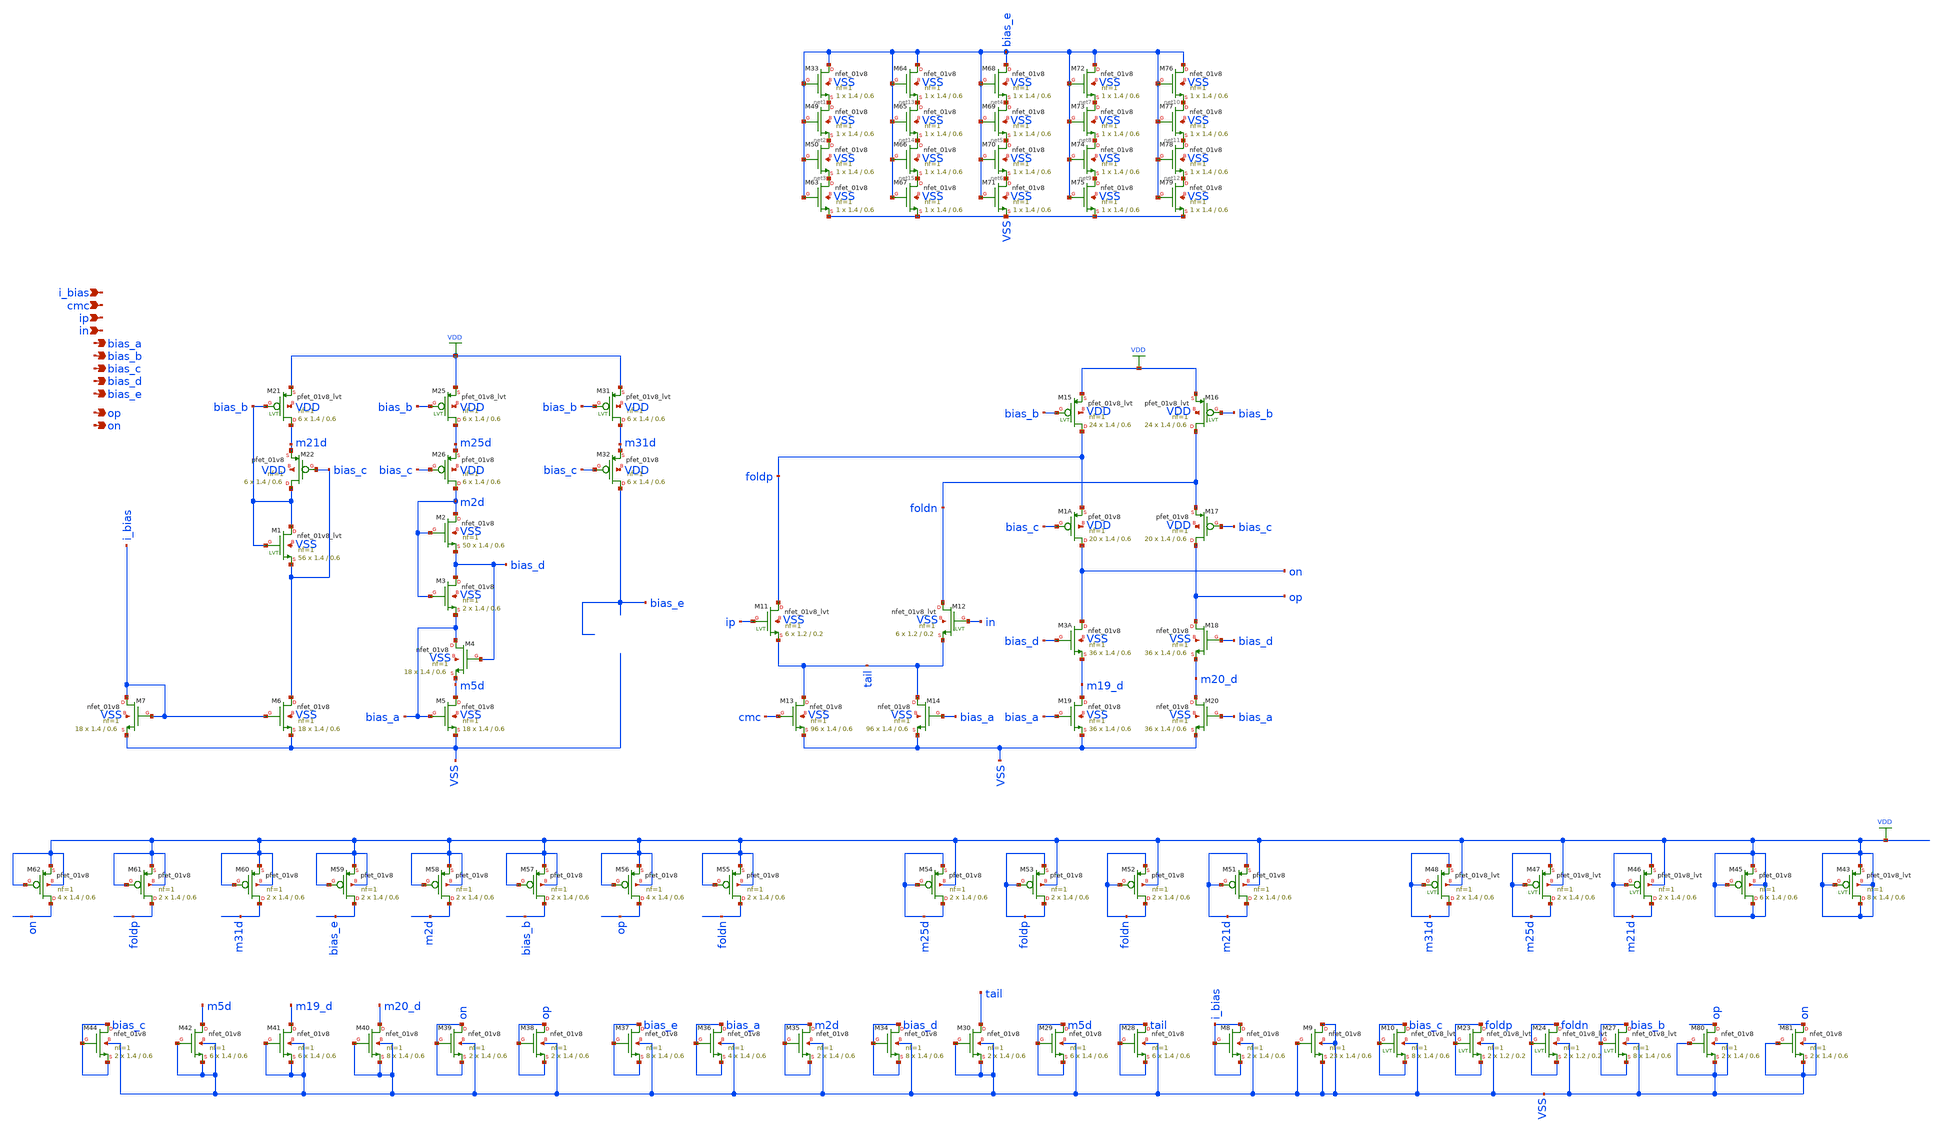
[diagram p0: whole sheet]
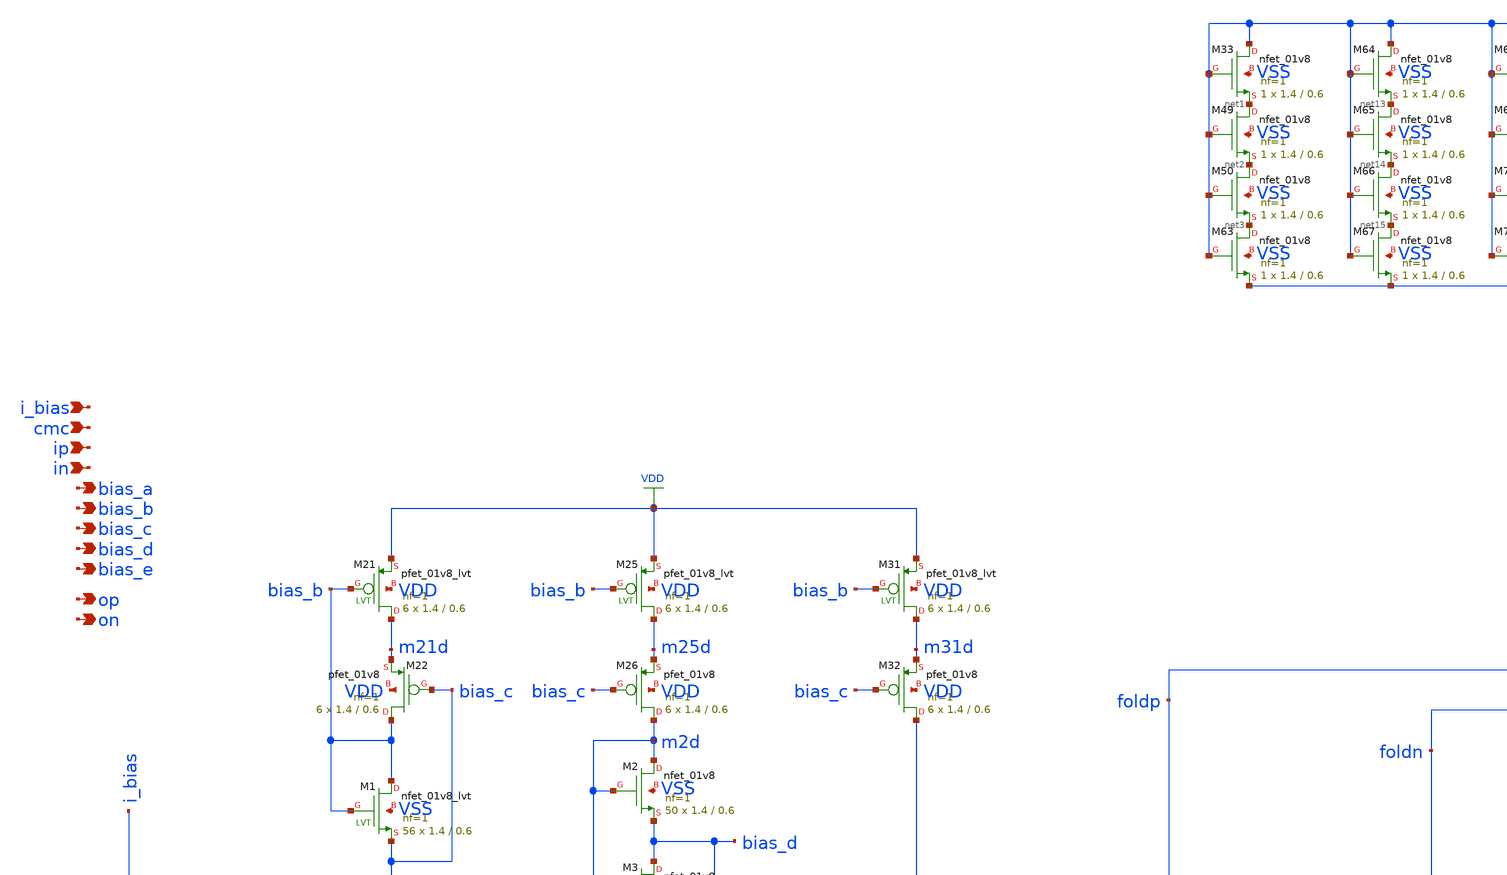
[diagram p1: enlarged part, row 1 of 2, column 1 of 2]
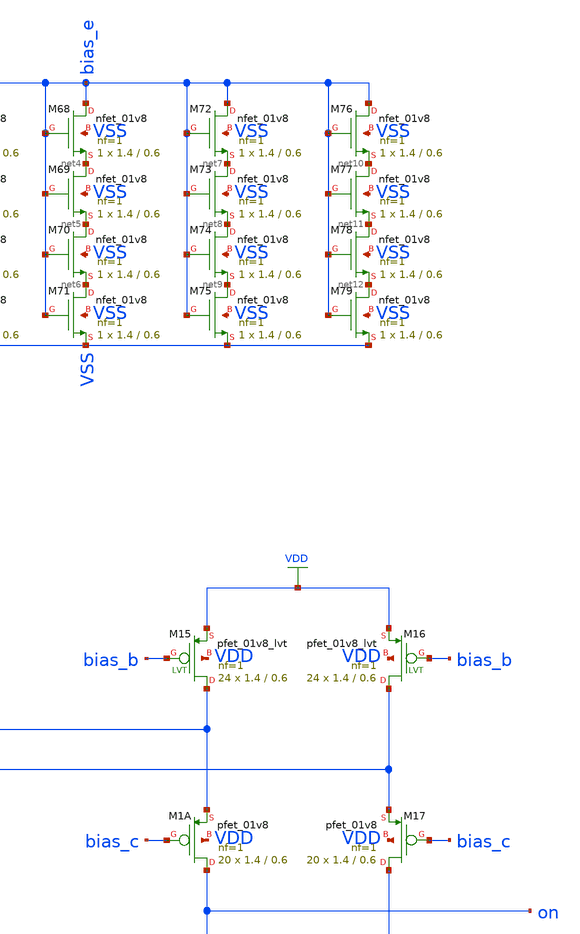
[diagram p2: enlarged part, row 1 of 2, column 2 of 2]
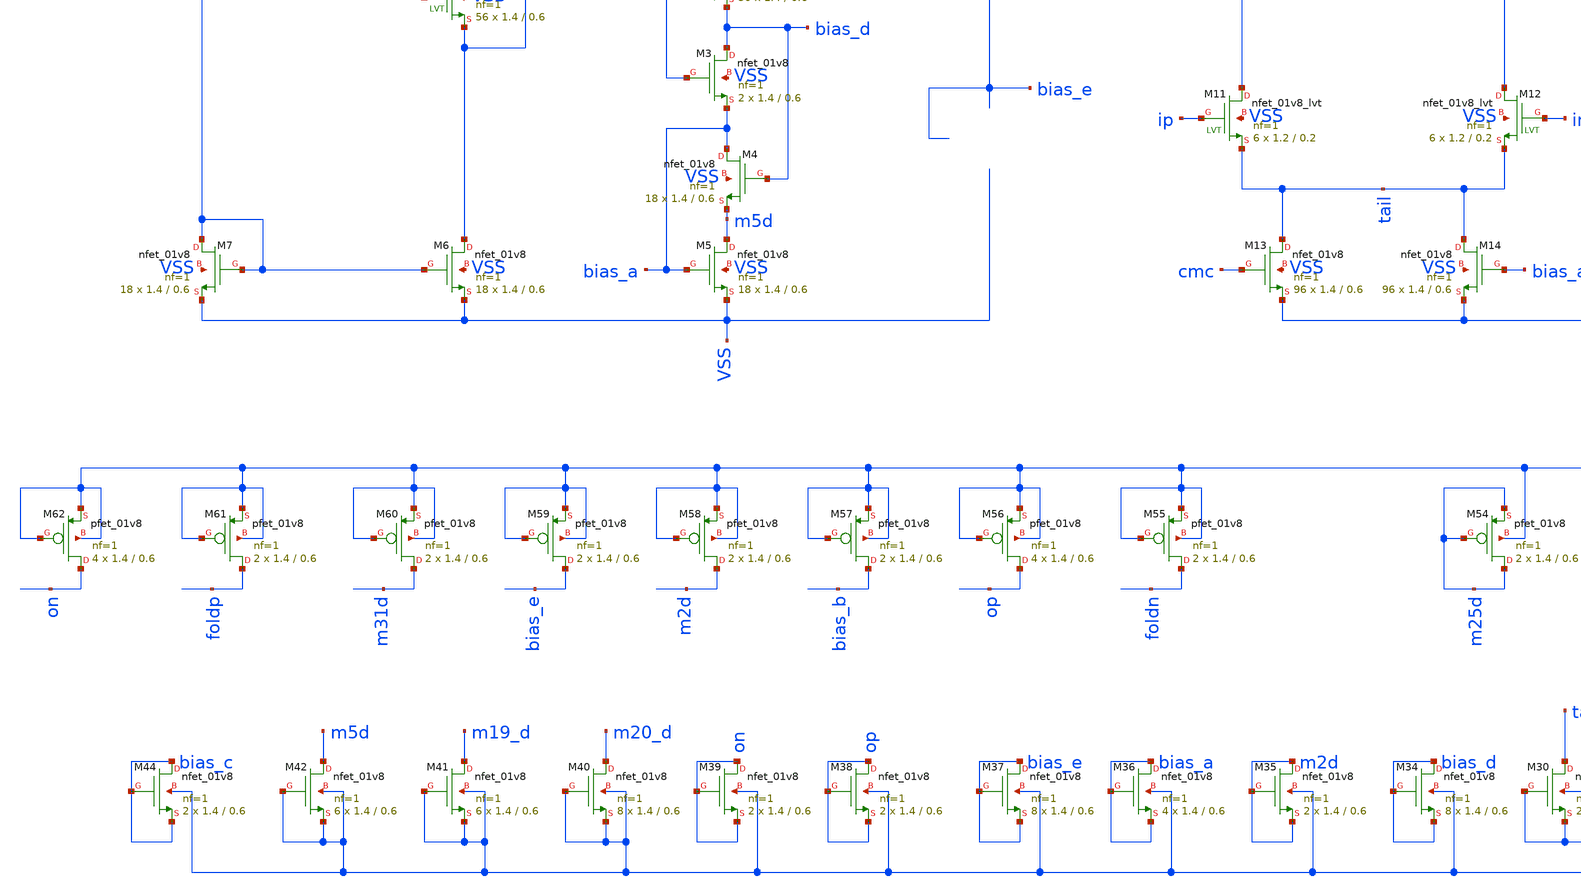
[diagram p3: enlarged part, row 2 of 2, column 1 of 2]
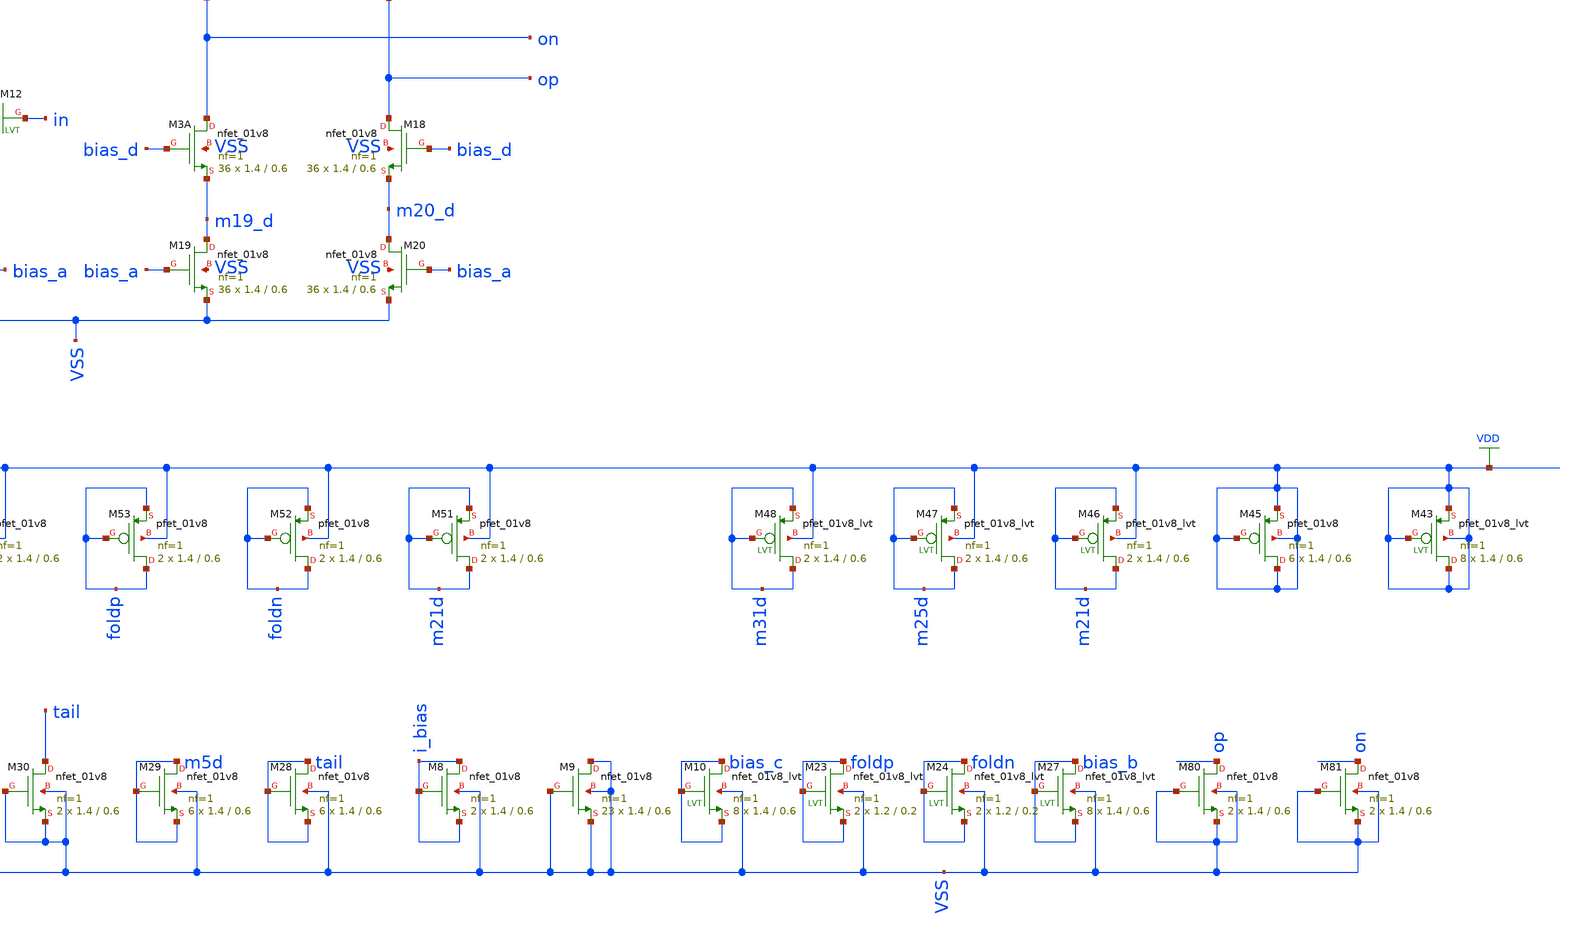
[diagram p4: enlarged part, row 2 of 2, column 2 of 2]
** sch_path: design/analog_modulator/schematic/ota_lvs.sch
**.subckt ota_lvs ip in op on i_bias bias_e bias_a bias_b bias_c bias_d cmc
*.ipin ip
*.ipin in
*.opin op
*.opin on
*.ipin i_bias
*.opin bias_e
*.opin bias_a
*.opin bias_b
*.opin bias_c
*.opin bias_d
*.ipin cmc
XM22 bias_b bias_c m21d VDD sky130_fd_pr__pfet_01v8 L=0.6 W=1.4 nf=1 ad='int((nf+1)/2) * W/nf * 0.29'
+ as='int((nf+2)/2) * W/nf * 0.29' pd='2*int((nf+1)/2) * (W/nf + 0.29)' ps='2*int((nf+2)/2) * (W/nf + 0.29)'
+ nrd='0.29 / W' nrs='0.29 / W' sa=0 sb=0 sd=0 mult=6 m=6
XM26 m2d bias_c m25d VDD sky130_fd_pr__pfet_01v8 L=0.6 W=1.4 nf=1 ad='int((nf+1)/2) * W/nf * 0.29' as='int((nf+2)/2) * W/nf * 0.29'
+ pd='2*int((nf+1)/2) * (W/nf + 0.29)' ps='2*int((nf+2)/2) * (W/nf + 0.29)' nrd='0.29 / W' nrs='0.29 / W'
+ sa=0 sb=0 sd=0 mult=6 m=6
XM32 bias_e bias_c m31d VDD sky130_fd_pr__pfet_01v8 L=0.6 W=1.4 nf=1 ad='int((nf+1)/2) * W/nf * 0.29'
+ as='int((nf+2)/2) * W/nf * 0.29' pd='2*int((nf+1)/2) * (W/nf + 0.29)' ps='2*int((nf+2)/2) * (W/nf + 0.29)'
+ nrd='0.29 / W' nrs='0.29 / W' sa=0 sb=0 sd=0 mult=6 m=6
XM33 bias_e bias_e net1 VSS sky130_fd_pr__nfet_01v8 L=0.6 W=1.4 nf=1 ad='int((nf+1)/2) * W/nf * 0.29'
+ as='int((nf+2)/2) * W/nf * 0.29' pd='2*int((nf+1)/2) * (W/nf + 0.29)' ps='2*int((nf+2)/2) * (W/nf + 0.29)'
+ nrd='0.29 / W' nrs='0.29 / W' sa=0 sb=0 sd=0 mult=1 m=1
XM21 m21d bias_b VDD VDD sky130_fd_pr__pfet_01v8_lvt L=0.6 W=1.4 nf=1 ad='int((nf+1)/2) * W/nf * 0.29'
+ as='int((nf+2)/2) * W/nf * 0.29' pd='2*int((nf+1)/2) * (W/nf + 0.29)' ps='2*int((nf+2)/2) * (W/nf + 0.29)'
+ nrd='0.29 / W' nrs='0.29 / W' sa=0 sb=0 sd=0 mult=6 m=6
XM25 m25d bias_b VDD VDD sky130_fd_pr__pfet_01v8_lvt L=0.6 W=1.4 nf=1 ad='int((nf+1)/2) * W/nf * 0.29'
+ as='int((nf+2)/2) * W/nf * 0.29' pd='2*int((nf+1)/2) * (W/nf + 0.29)' ps='2*int((nf+2)/2) * (W/nf + 0.29)'
+ nrd='0.29 / W' nrs='0.29 / W' sa=0 sb=0 sd=0 mult=6 m=6
XM31 m31d bias_b VDD VDD sky130_fd_pr__pfet_01v8_lvt L=0.6 W=1.4 nf=1 ad='int((nf+1)/2) * W/nf * 0.29'
+ as='int((nf+2)/2) * W/nf * 0.29' pd='2*int((nf+1)/2) * (W/nf + 0.29)' ps='2*int((nf+2)/2) * (W/nf + 0.29)'
+ nrd='0.29 / W' nrs='0.29 / W' sa=0 sb=0 sd=0 mult=6 m=6
XM1 bias_b bias_b bias_c VSS sky130_fd_pr__nfet_01v8_lvt L=0.6 W=1.4 nf=1 ad='int((nf+1)/2) * W/nf * 0.29'
+ as='int((nf+2)/2) * W/nf * 0.29' pd='2*int((nf+1)/2) * (W/nf + 0.29)' ps='2*int((nf+2)/2) * (W/nf + 0.29)'
+ nrd='0.29 / W' nrs='0.29 / W' sa=0 sb=0 sd=0 mult=56 m=56
XM2 m2d m2d bias_d VSS sky130_fd_pr__nfet_01v8 L=0.6 W=1.4 nf=1 ad='int((nf+1)/2) * W/nf * 0.29' as='int((nf+2)/2) * W/nf * 0.29'
+ pd='2*int((nf+1)/2) * (W/nf + 0.29)' ps='2*int((nf+2)/2) * (W/nf + 0.29)' nrd='0.29 / W' nrs='0.29 / W'
+ sa=0 sb=0 sd=0 mult=50 m=50
XM3 bias_d m2d bias_a VSS sky130_fd_pr__nfet_01v8 L=0.6 W=1.4 nf=1 ad='int((nf+1)/2) * W/nf * 0.29' as='int((nf+2)/2) * W/nf * 0.29'
+ pd='2*int((nf+1)/2) * (W/nf + 0.29)' ps='2*int((nf+2)/2) * (W/nf + 0.29)' nrd='0.29 / W' nrs='0.29 / W'
+ sa=0 sb=0 sd=0 mult=2 m=2
XM4 bias_a bias_d m5d VSS sky130_fd_pr__nfet_01v8 L=0.6 W=1.4 nf=1 ad='int((nf+1)/2) * W/nf * 0.29' as='int((nf+2)/2) * W/nf * 0.29'
+ pd='2*int((nf+1)/2) * (W/nf + 0.29)' ps='2*int((nf+2)/2) * (W/nf + 0.29)' nrd='0.29 / W' nrs='0.29 / W'
+ sa=0 sb=0 sd=0 mult=18 m=18
XM5 m5d bias_a VSS VSS sky130_fd_pr__nfet_01v8 L=0.6 W=1.4 nf=1 ad='int((nf+1)/2) * W/nf * 0.29' as='int((nf+2)/2) * W/nf * 0.29'
+ pd='2*int((nf+1)/2) * (W/nf + 0.29)' ps='2*int((nf+2)/2) * (W/nf + 0.29)' nrd='0.29 / W' nrs='0.29 / W'
+ sa=0 sb=0 sd=0 mult=18 m=18
XM6 bias_c i_bias VSS VSS sky130_fd_pr__nfet_01v8 L=0.6 W=1.4 nf=1 ad='int((nf+1)/2) * W/nf * 0.29' as='int((nf+2)/2) * W/nf * 0.29'
+ pd='2*int((nf+1)/2) * (W/nf + 0.29)' ps='2*int((nf+2)/2) * (W/nf + 0.29)' nrd='0.29 / W' nrs='0.29 / W'
+ sa=0 sb=0 sd=0 mult=18 m=18
XM7 i_bias i_bias VSS VSS sky130_fd_pr__nfet_01v8 L=0.6 W=1.4 nf=1 ad='int((nf+1)/2) * W/nf * 0.29' as='int((nf+2)/2) * W/nf * 0.29'
+ pd='2*int((nf+1)/2) * (W/nf + 0.29)' ps='2*int((nf+2)/2) * (W/nf + 0.29)' nrd='0.29 / W' nrs='0.29 / W'
+ sa=0 sb=0 sd=0 mult=18 m=18
XM8 i_bias i_bias i_bias VSS sky130_fd_pr__nfet_01v8 L=0.6 W=1.4 nf=1 ad='int((nf+1)/2) * W/nf * 0.29'
+ as='int((nf+2)/2) * W/nf * 0.29' pd='2*int((nf+1)/2) * (W/nf + 0.29)' ps='2*int((nf+2)/2) * (W/nf + 0.29)'
+ nrd='0.29 / W' nrs='0.29 / W' sa=0 sb=0 sd=0 mult=2 m=2
XM9 VSS VSS VSS VSS sky130_fd_pr__nfet_01v8 L=0.6 W=1.4 nf=1 ad='int((nf+1)/2) * W/nf * 0.29' as='int((nf+2)/2) * W/nf * 0.29'
+ pd='2*int((nf+1)/2) * (W/nf + 0.29)' ps='2*int((nf+2)/2) * (W/nf + 0.29)' nrd='0.29 / W' nrs='0.29 / W'
+ sa=0 sb=0 sd=0 mult=23 m=23
XM10 bias_c bias_c bias_c VSS sky130_fd_pr__nfet_01v8_lvt L=0.6 W=1.4 nf=1 ad='int((nf+1)/2) * W/nf * 0.29'
+ as='int((nf+2)/2) * W/nf * 0.29' pd='2*int((nf+1)/2) * (W/nf + 0.29)' ps='2*int((nf+2)/2) * (W/nf + 0.29)'
+ nrd='0.29 / W' nrs='0.29 / W' sa=0 sb=0 sd=0 mult=8 m=8
XM11 foldp ip tail VSS sky130_fd_pr__nfet_01v8_lvt L=0.2 W=1.2 nf=1 ad='int((nf+1)/2) * W/nf * 0.29'
+ as='int((nf+2)/2) * W/nf * 0.29' pd='2*int((nf+1)/2) * (W/nf + 0.29)' ps='2*int((nf+2)/2) * (W/nf + 0.29)'
+ nrd='0.29 / W' nrs='0.29 / W' sa=0 sb=0 sd=0 mult=6 m=6
XM12 foldn in tail VSS sky130_fd_pr__nfet_01v8_lvt L=0.2 W=1.2 nf=1 ad='int((nf+1)/2) * W/nf * 0.29'
+ as='int((nf+2)/2) * W/nf * 0.29' pd='2*int((nf+1)/2) * (W/nf + 0.29)' ps='2*int((nf+2)/2) * (W/nf + 0.29)'
+ nrd='0.29 / W' nrs='0.29 / W' sa=0 sb=0 sd=0 mult=6 m=6
XM13 tail cmc VSS VSS sky130_fd_pr__nfet_01v8 L=0.6 W=1.4 nf=1 ad='int((nf+1)/2) * W/nf * 0.29' as='int((nf+2)/2) * W/nf * 0.29'
+ pd='2*int((nf+1)/2) * (W/nf + 0.29)' ps='2*int((nf+2)/2) * (W/nf + 0.29)' nrd='0.29 / W' nrs='0.29 / W'
+ sa=0 sb=0 sd=0 mult=96 m=96
XM14 tail bias_a VSS VSS sky130_fd_pr__nfet_01v8 L=0.6 W=1.4 nf=1 ad='int((nf+1)/2) * W/nf * 0.29' as='int((nf+2)/2) * W/nf * 0.29'
+ pd='2*int((nf+1)/2) * (W/nf + 0.29)' ps='2*int((nf+2)/2) * (W/nf + 0.29)' nrd='0.29 / W' nrs='0.29 / W'
+ sa=0 sb=0 sd=0 mult=96 m=96
XM15 foldp bias_b VDD VDD sky130_fd_pr__pfet_01v8_lvt L=0.6 W=1.4 nf=1 ad='int((nf+1)/2) * W/nf * 0.29'
+ as='int((nf+2)/2) * W/nf * 0.29' pd='2*int((nf+1)/2) * (W/nf + 0.29)' ps='2*int((nf+2)/2) * (W/nf + 0.29)'
+ nrd='0.29 / W' nrs='0.29 / W' sa=0 sb=0 sd=0 mult=24 m=24
XM16 foldn bias_b VDD VDD sky130_fd_pr__pfet_01v8_lvt L=0.6 W=1.4 nf=1 ad='int((nf+1)/2) * W/nf * 0.29'
+ as='int((nf+2)/2) * W/nf * 0.29' pd='2*int((nf+1)/2) * (W/nf + 0.29)' ps='2*int((nf+2)/2) * (W/nf + 0.29)'
+ nrd='0.29 / W' nrs='0.29 / W' sa=0 sb=0 sd=0 mult=24 m=24
XM1A on bias_c foldp VDD sky130_fd_pr__pfet_01v8 L=0.6 W=1.4 nf=1 ad='int((nf+1)/2) * W/nf * 0.29' as='int((nf+2)/2) * W/nf * 0.29'
+ pd='2*int((nf+1)/2) * (W/nf + 0.29)' ps='2*int((nf+2)/2) * (W/nf + 0.29)' nrd='0.29 / W' nrs='0.29 / W'
+ sa=0 sb=0 sd=0 mult=20 m=20
XM17 op bias_c foldn VDD sky130_fd_pr__pfet_01v8 L=0.6 W=1.4 nf=1 ad='int((nf+1)/2) * W/nf * 0.29' as='int((nf+2)/2) * W/nf * 0.29'
+ pd='2*int((nf+1)/2) * (W/nf + 0.29)' ps='2*int((nf+2)/2) * (W/nf + 0.29)' nrd='0.29 / W' nrs='0.29 / W'
+ sa=0 sb=0 sd=0 mult=20 m=20
XM3A on bias_d m19_d VSS sky130_fd_pr__nfet_01v8 L=0.6 W=1.4 nf=1 ad='int((nf+1)/2) * W/nf * 0.29' as='int((nf+2)/2) * W/nf * 0.29'
+ pd='2*int((nf+1)/2) * (W/nf + 0.29)' ps='2*int((nf+2)/2) * (W/nf + 0.29)' nrd='0.29 / W' nrs='0.29 / W'
+ sa=0 sb=0 sd=0 mult=36 m=36
XM18 op bias_d m20_d VSS sky130_fd_pr__nfet_01v8 L=0.6 W=1.4 nf=1 ad='int((nf+1)/2) * W/nf * 0.29' as='int((nf+2)/2) * W/nf * 0.29'
+ pd='2*int((nf+1)/2) * (W/nf + 0.29)' ps='2*int((nf+2)/2) * (W/nf + 0.29)' nrd='0.29 / W' nrs='0.29 / W'
+ sa=0 sb=0 sd=0 mult=36 m=36
XM19 m19_d bias_a VSS VSS sky130_fd_pr__nfet_01v8 L=0.6 W=1.4 nf=1 ad='int((nf+1)/2) * W/nf * 0.29' as='int((nf+2)/2) * W/nf * 0.29'
+ pd='2*int((nf+1)/2) * (W/nf + 0.29)' ps='2*int((nf+2)/2) * (W/nf + 0.29)' nrd='0.29 / W' nrs='0.29 / W'
+ sa=0 sb=0 sd=0 mult=36 m=36
XM20 m20_d bias_a VSS VSS sky130_fd_pr__nfet_01v8 L=0.6 W=1.4 nf=1 ad='int((nf+1)/2) * W/nf * 0.29' as='int((nf+2)/2) * W/nf * 0.29'
+ pd='2*int((nf+1)/2) * (W/nf + 0.29)' ps='2*int((nf+2)/2) * (W/nf + 0.29)' nrd='0.29 / W' nrs='0.29 / W'
+ sa=0 sb=0 sd=0 mult=36 m=36
XM23 foldp foldp foldp VSS sky130_fd_pr__nfet_01v8_lvt L=0.2 W=1.2 nf=1 ad='int((nf+1)/2) * W/nf * 0.29'
+ as='int((nf+2)/2) * W/nf * 0.29' pd='2*int((nf+1)/2) * (W/nf + 0.29)' ps='2*int((nf+2)/2) * (W/nf + 0.29)'
+ nrd='0.29 / W' nrs='0.29 / W' sa=0 sb=0 sd=0 mult=2 m=2
XM24 foldn foldn foldn VSS sky130_fd_pr__nfet_01v8_lvt L=0.2 W=1.2 nf=1 ad='int((nf+1)/2) * W/nf * 0.29'
+ as='int((nf+2)/2) * W/nf * 0.29' pd='2*int((nf+1)/2) * (W/nf + 0.29)' ps='2*int((nf+2)/2) * (W/nf + 0.29)'
+ nrd='0.29 / W' nrs='0.29 / W' sa=0 sb=0 sd=0 mult=2 m=2
XM27 bias_b bias_b bias_b VSS sky130_fd_pr__nfet_01v8_lvt L=0.6 W=1.4 nf=1 ad='int((nf+1)/2) * W/nf * 0.29'
+ as='int((nf+2)/2) * W/nf * 0.29' pd='2*int((nf+1)/2) * (W/nf + 0.29)' ps='2*int((nf+2)/2) * (W/nf + 0.29)'
+ nrd='0.29 / W' nrs='0.29 / W' sa=0 sb=0 sd=0 mult=8 m=8
XM28 tail tail tail VSS sky130_fd_pr__nfet_01v8 L=0.6 W=1.4 nf=1 ad='int((nf+1)/2) * W/nf * 0.29' as='int((nf+2)/2) * W/nf * 0.29'
+ pd='2*int((nf+1)/2) * (W/nf + 0.29)' ps='2*int((nf+2)/2) * (W/nf + 0.29)' nrd='0.29 / W' nrs='0.29 / W'
+ sa=0 sb=0 sd=0 mult=6 m=6
XM29 m5d m5d m5d VSS sky130_fd_pr__nfet_01v8 L=0.6 W=1.4 nf=1 ad='int((nf+1)/2) * W/nf * 0.29' as='int((nf+2)/2) * W/nf * 0.29'
+ pd='2*int((nf+1)/2) * (W/nf + 0.29)' ps='2*int((nf+2)/2) * (W/nf + 0.29)' nrd='0.29 / W' nrs='0.29 / W'
+ sa=0 sb=0 sd=0 mult=6 m=6
XM30 tail VSS VSS VSS sky130_fd_pr__nfet_01v8 L=0.6 W=1.4 nf=1 ad='int((nf+1)/2) * W/nf * 0.29' as='int((nf+2)/2) * W/nf * 0.29'
+ pd='2*int((nf+1)/2) * (W/nf + 0.29)' ps='2*int((nf+2)/2) * (W/nf + 0.29)' nrd='0.29 / W' nrs='0.29 / W'
+ sa=0 sb=0 sd=0 mult=2 m=2
XM34 bias_d bias_d bias_d VSS sky130_fd_pr__nfet_01v8 L=0.6 W=1.4 nf=1 ad='int((nf+1)/2) * W/nf * 0.29'
+ as='int((nf+2)/2) * W/nf * 0.29' pd='2*int((nf+1)/2) * (W/nf + 0.29)' ps='2*int((nf+2)/2) * (W/nf + 0.29)'
+ nrd='0.29 / W' nrs='0.29 / W' sa=0 sb=0 sd=0 mult=8 m=8
XM35 m2d m2d m2d VSS sky130_fd_pr__nfet_01v8 L=0.6 W=1.4 nf=1 ad='int((nf+1)/2) * W/nf * 0.29' as='int((nf+2)/2) * W/nf * 0.29'
+ pd='2*int((nf+1)/2) * (W/nf + 0.29)' ps='2*int((nf+2)/2) * (W/nf + 0.29)' nrd='0.29 / W' nrs='0.29 / W'
+ sa=0 sb=0 sd=0 mult=2 m=2
XM36 bias_a bias_a bias_a VSS sky130_fd_pr__nfet_01v8 L=0.6 W=1.4 nf=1 ad='int((nf+1)/2) * W/nf * 0.29'
+ as='int((nf+2)/2) * W/nf * 0.29' pd='2*int((nf+1)/2) * (W/nf + 0.29)' ps='2*int((nf+2)/2) * (W/nf + 0.29)'
+ nrd='0.29 / W' nrs='0.29 / W' sa=0 sb=0 sd=0 mult=4 m=4
XM37 bias_e bias_e bias_e VSS sky130_fd_pr__nfet_01v8 L=0.6 W=1.4 nf=1 ad='int((nf+1)/2) * W/nf * 0.29'
+ as='int((nf+2)/2) * W/nf * 0.29' pd='2*int((nf+1)/2) * (W/nf + 0.29)' ps='2*int((nf+2)/2) * (W/nf + 0.29)'
+ nrd='0.29 / W' nrs='0.29 / W' sa=0 sb=0 sd=0 mult=8 m=8
XM38 op op op VSS sky130_fd_pr__nfet_01v8 L=0.6 W=1.4 nf=1 ad='int((nf+1)/2) * W/nf * 0.29' as='int((nf+2)/2) * W/nf * 0.29'
+ pd='2*int((nf+1)/2) * (W/nf + 0.29)' ps='2*int((nf+2)/2) * (W/nf + 0.29)' nrd='0.29 / W' nrs='0.29 / W'
+ sa=0 sb=0 sd=0 mult=2 m=2
XM39 on on on VSS sky130_fd_pr__nfet_01v8 L=0.6 W=1.4 nf=1 ad='int((nf+1)/2) * W/nf * 0.29' as='int((nf+2)/2) * W/nf * 0.29'
+ pd='2*int((nf+1)/2) * (W/nf + 0.29)' ps='2*int((nf+2)/2) * (W/nf + 0.29)' nrd='0.29 / W' nrs='0.29 / W'
+ sa=0 sb=0 sd=0 mult=2 m=2
XM40 m20_d VSS VSS VSS sky130_fd_pr__nfet_01v8 L=0.6 W=1.4 nf=1 ad='int((nf+1)/2) * W/nf * 0.29' as='int((nf+2)/2) * W/nf * 0.29'
+ pd='2*int((nf+1)/2) * (W/nf + 0.29)' ps='2*int((nf+2)/2) * (W/nf + 0.29)' nrd='0.29 / W' nrs='0.29 / W'
+ sa=0 sb=0 sd=0 mult=8 m=8
XM41 m19_d VSS VSS VSS sky130_fd_pr__nfet_01v8 L=0.6 W=1.4 nf=1 ad='int((nf+1)/2) * W/nf * 0.29' as='int((nf+2)/2) * W/nf * 0.29'
+ pd='2*int((nf+1)/2) * (W/nf + 0.29)' ps='2*int((nf+2)/2) * (W/nf + 0.29)' nrd='0.29 / W' nrs='0.29 / W'
+ sa=0 sb=0 sd=0 mult=6 m=6
XM42 m5d VSS VSS VSS sky130_fd_pr__nfet_01v8 L=0.6 W=1.4 nf=1 ad='int((nf+1)/2) * W/nf * 0.29' as='int((nf+2)/2) * W/nf * 0.29'
+ pd='2*int((nf+1)/2) * (W/nf + 0.29)' ps='2*int((nf+2)/2) * (W/nf + 0.29)' nrd='0.29 / W' nrs='0.29 / W'
+ sa=0 sb=0 sd=0 mult=6 m=6
XM43 VDD VDD VDD VDD sky130_fd_pr__pfet_01v8_lvt L=0.6 W=1.4 nf=1 ad='int((nf+1)/2) * W/nf * 0.29' as='int((nf+2)/2) * W/nf * 0.29'
+ pd='2*int((nf+1)/2) * (W/nf + 0.29)' ps='2*int((nf+2)/2) * (W/nf + 0.29)' nrd='0.29 / W' nrs='0.29 / W'
+ sa=0 sb=0 sd=0 mult=8 m=8
XM44 bias_c bias_c bias_c VSS sky130_fd_pr__nfet_01v8 L=0.6 W=1.4 nf=1 ad='int((nf+1)/2) * W/nf * 0.29'
+ as='int((nf+2)/2) * W/nf * 0.29' pd='2*int((nf+1)/2) * (W/nf + 0.29)' ps='2*int((nf+2)/2) * (W/nf + 0.29)'
+ nrd='0.29 / W' nrs='0.29 / W' sa=0 sb=0 sd=0 mult=2 m=2
XM45 VDD VDD VDD VDD sky130_fd_pr__pfet_01v8 L=0.6 W=1.4 nf=1 ad='int((nf+1)/2) * W/nf * 0.29' as='int((nf+2)/2) * W/nf * 0.29'
+ pd='2*int((nf+1)/2) * (W/nf + 0.29)' ps='2*int((nf+2)/2) * (W/nf + 0.29)' nrd='0.29 / W' nrs='0.29 / W'
+ sa=0 sb=0 sd=0 mult=6 m=6
XM46 m21d m21d m21d VDD sky130_fd_pr__pfet_01v8_lvt L=0.6 W=1.4 nf=1 ad='int((nf+1)/2) * W/nf * 0.29'
+ as='int((nf+2)/2) * W/nf * 0.29' pd='2*int((nf+1)/2) * (W/nf + 0.29)' ps='2*int((nf+2)/2) * (W/nf + 0.29)'
+ nrd='0.29 / W' nrs='0.29 / W' sa=0 sb=0 sd=0 mult=2 m=2
XM47 m25d m25d m25d VDD sky130_fd_pr__pfet_01v8_lvt L=0.6 W=1.4 nf=1 ad='int((nf+1)/2) * W/nf * 0.29'
+ as='int((nf+2)/2) * W/nf * 0.29' pd='2*int((nf+1)/2) * (W/nf + 0.29)' ps='2*int((nf+2)/2) * (W/nf + 0.29)'
+ nrd='0.29 / W' nrs='0.29 / W' sa=0 sb=0 sd=0 mult=2 m=2
XM48 m31d m31d m31d VDD sky130_fd_pr__pfet_01v8_lvt L=0.6 W=1.4 nf=1 ad='int((nf+1)/2) * W/nf * 0.29'
+ as='int((nf+2)/2) * W/nf * 0.29' pd='2*int((nf+1)/2) * (W/nf + 0.29)' ps='2*int((nf+2)/2) * (W/nf + 0.29)'
+ nrd='0.29 / W' nrs='0.29 / W' sa=0 sb=0 sd=0 mult=2 m=2
XM51 m21d m21d m21d VDD sky130_fd_pr__pfet_01v8 L=0.6 W=1.4 nf=1 ad='int((nf+1)/2) * W/nf * 0.29' as='int((nf+2)/2) * W/nf * 0.29'
+ pd='2*int((nf+1)/2) * (W/nf + 0.29)' ps='2*int((nf+2)/2) * (W/nf + 0.29)' nrd='0.29 / W' nrs='0.29 / W'
+ sa=0 sb=0 sd=0 mult=2 m=2
XM52 foldn foldn foldn VDD sky130_fd_pr__pfet_01v8 L=0.6 W=1.4 nf=1 ad='int((nf+1)/2) * W/nf * 0.29'
+ as='int((nf+2)/2) * W/nf * 0.29' pd='2*int((nf+1)/2) * (W/nf + 0.29)' ps='2*int((nf+2)/2) * (W/nf + 0.29)'
+ nrd='0.29 / W' nrs='0.29 / W' sa=0 sb=0 sd=0 mult=2 m=2
XM53 foldp foldp foldp VDD sky130_fd_pr__pfet_01v8 L=0.6 W=1.4 nf=1 ad='int((nf+1)/2) * W/nf * 0.29'
+ as='int((nf+2)/2) * W/nf * 0.29' pd='2*int((nf+1)/2) * (W/nf + 0.29)' ps='2*int((nf+2)/2) * (W/nf + 0.29)'
+ nrd='0.29 / W' nrs='0.29 / W' sa=0 sb=0 sd=0 mult=2 m=2
XM54 m25d m25d m25d VDD sky130_fd_pr__pfet_01v8 L=0.6 W=1.4 nf=1 ad='int((nf+1)/2) * W/nf * 0.29' as='int((nf+2)/2) * W/nf * 0.29'
+ pd='2*int((nf+1)/2) * (W/nf + 0.29)' ps='2*int((nf+2)/2) * (W/nf + 0.29)' nrd='0.29 / W' nrs='0.29 / W'
+ sa=0 sb=0 sd=0 mult=2 m=2
XM55 foldn VDD VDD VDD sky130_fd_pr__pfet_01v8 L=0.6 W=1.4 nf=1 ad='int((nf+1)/2) * W/nf * 0.29' as='int((nf+2)/2) * W/nf * 0.29'
+ pd='2*int((nf+1)/2) * (W/nf + 0.29)' ps='2*int((nf+2)/2) * (W/nf + 0.29)' nrd='0.29 / W' nrs='0.29 / W'
+ sa=0 sb=0 sd=0 mult=2 m=2
XM56 op VDD VDD VDD sky130_fd_pr__pfet_01v8 L=0.6 W=1.4 nf=1 ad='int((nf+1)/2) * W/nf * 0.29' as='int((nf+2)/2) * W/nf * 0.29'
+ pd='2*int((nf+1)/2) * (W/nf + 0.29)' ps='2*int((nf+2)/2) * (W/nf + 0.29)' nrd='0.29 / W' nrs='0.29 / W'
+ sa=0 sb=0 sd=0 mult=4 m=4
XM57 bias_b VDD VDD VDD sky130_fd_pr__pfet_01v8 L=0.6 W=1.4 nf=1 ad='int((nf+1)/2) * W/nf * 0.29' as='int((nf+2)/2) * W/nf * 0.29'
+ pd='2*int((nf+1)/2) * (W/nf + 0.29)' ps='2*int((nf+2)/2) * (W/nf + 0.29)' nrd='0.29 / W' nrs='0.29 / W'
+ sa=0 sb=0 sd=0 mult=2 m=2
XM58 m2d VDD VDD VDD sky130_fd_pr__pfet_01v8 L=0.6 W=1.4 nf=1 ad='int((nf+1)/2) * W/nf * 0.29' as='int((nf+2)/2) * W/nf * 0.29'
+ pd='2*int((nf+1)/2) * (W/nf + 0.29)' ps='2*int((nf+2)/2) * (W/nf + 0.29)' nrd='0.29 / W' nrs='0.29 / W'
+ sa=0 sb=0 sd=0 mult=2 m=2
XM59 bias_e VDD VDD VDD sky130_fd_pr__pfet_01v8 L=0.6 W=1.4 nf=1 ad='int((nf+1)/2) * W/nf * 0.29' as='int((nf+2)/2) * W/nf * 0.29'
+ pd='2*int((nf+1)/2) * (W/nf + 0.29)' ps='2*int((nf+2)/2) * (W/nf + 0.29)' nrd='0.29 / W' nrs='0.29 / W'
+ sa=0 sb=0 sd=0 mult=2 m=2
XM60 m31d VDD VDD VDD sky130_fd_pr__pfet_01v8 L=0.6 W=1.4 nf=1 ad='int((nf+1)/2) * W/nf * 0.29' as='int((nf+2)/2) * W/nf * 0.29'
+ pd='2*int((nf+1)/2) * (W/nf + 0.29)' ps='2*int((nf+2)/2) * (W/nf + 0.29)' nrd='0.29 / W' nrs='0.29 / W'
+ sa=0 sb=0 sd=0 mult=2 m=2
XM61 foldp VDD VDD VDD sky130_fd_pr__pfet_01v8 L=0.6 W=1.4 nf=1 ad='int((nf+1)/2) * W/nf * 0.29' as='int((nf+2)/2) * W/nf * 0.29'
+ pd='2*int((nf+1)/2) * (W/nf + 0.29)' ps='2*int((nf+2)/2) * (W/nf + 0.29)' nrd='0.29 / W' nrs='0.29 / W'
+ sa=0 sb=0 sd=0 mult=2 m=2
XM62 on VDD VDD VDD sky130_fd_pr__pfet_01v8 L=0.6 W=1.4 nf=1 ad='int((nf+1)/2) * W/nf * 0.29' as='int((nf+2)/2) * W/nf * 0.29'
+ pd='2*int((nf+1)/2) * (W/nf + 0.29)' ps='2*int((nf+2)/2) * (W/nf + 0.29)' nrd='0.29 / W' nrs='0.29 / W'
+ sa=0 sb=0 sd=0 mult=4 m=4
XM49 net1 bias_e net2 VSS sky130_fd_pr__nfet_01v8 L=0.6 W=1.4 nf=1 ad='int((nf+1)/2) * W/nf * 0.29' as='int((nf+2)/2) * W/nf * 0.29'
+ pd='2*int((nf+1)/2) * (W/nf + 0.29)' ps='2*int((nf+2)/2) * (W/nf + 0.29)' nrd='0.29 / W' nrs='0.29 / W'
+ sa=0 sb=0 sd=0 mult=1 m=1
XM50 net2 bias_e net3 VSS sky130_fd_pr__nfet_01v8 L=0.6 W=1.4 nf=1 ad='int((nf+1)/2) * W/nf * 0.29' as='int((nf+2)/2) * W/nf * 0.29'
+ pd='2*int((nf+1)/2) * (W/nf + 0.29)' ps='2*int((nf+2)/2) * (W/nf + 0.29)' nrd='0.29 / W' nrs='0.29 / W'
+ sa=0 sb=0 sd=0 mult=1 m=1
XM63 net3 bias_e VSS VSS sky130_fd_pr__nfet_01v8 L=0.6 W=1.4 nf=1 ad='int((nf+1)/2) * W/nf * 0.29' as='int((nf+2)/2) * W/nf * 0.29'
+ pd='2*int((nf+1)/2) * (W/nf + 0.29)' ps='2*int((nf+2)/2) * (W/nf + 0.29)' nrd='0.29 / W' nrs='0.29 / W'
+ sa=0 sb=0 sd=0 mult=1 m=1
XM68 bias_e bias_e net4 VSS sky130_fd_pr__nfet_01v8 L=0.6 W=1.4 nf=1 ad='int((nf+1)/2) * W/nf * 0.29'
+ as='int((nf+2)/2) * W/nf * 0.29' pd='2*int((nf+1)/2) * (W/nf + 0.29)' ps='2*int((nf+2)/2) * (W/nf + 0.29)'
+ nrd='0.29 / W' nrs='0.29 / W' sa=0 sb=0 sd=0 mult=1 m=1
XM69 net4 bias_e net5 VSS sky130_fd_pr__nfet_01v8 L=0.6 W=1.4 nf=1 ad='int((nf+1)/2) * W/nf * 0.29' as='int((nf+2)/2) * W/nf * 0.29'
+ pd='2*int((nf+1)/2) * (W/nf + 0.29)' ps='2*int((nf+2)/2) * (W/nf + 0.29)' nrd='0.29 / W' nrs='0.29 / W'
+ sa=0 sb=0 sd=0 mult=1 m=1
XM70 net5 bias_e net6 VSS sky130_fd_pr__nfet_01v8 L=0.6 W=1.4 nf=1 ad='int((nf+1)/2) * W/nf * 0.29' as='int((nf+2)/2) * W/nf * 0.29'
+ pd='2*int((nf+1)/2) * (W/nf + 0.29)' ps='2*int((nf+2)/2) * (W/nf + 0.29)' nrd='0.29 / W' nrs='0.29 / W'
+ sa=0 sb=0 sd=0 mult=1 m=1
XM71 net6 bias_e VSS VSS sky130_fd_pr__nfet_01v8 L=0.6 W=1.4 nf=1 ad='int((nf+1)/2) * W/nf * 0.29' as='int((nf+2)/2) * W/nf * 0.29'
+ pd='2*int((nf+1)/2) * (W/nf + 0.29)' ps='2*int((nf+2)/2) * (W/nf + 0.29)' nrd='0.29 / W' nrs='0.29 / W'
+ sa=0 sb=0 sd=0 mult=1 m=1
XM72 bias_e bias_e net7 VSS sky130_fd_pr__nfet_01v8 L=0.6 W=1.4 nf=1 ad='int((nf+1)/2) * W/nf * 0.29'
+ as='int((nf+2)/2) * W/nf * 0.29' pd='2*int((nf+1)/2) * (W/nf + 0.29)' ps='2*int((nf+2)/2) * (W/nf + 0.29)'
+ nrd='0.29 / W' nrs='0.29 / W' sa=0 sb=0 sd=0 mult=1 m=1
XM73 net7 bias_e net8 VSS sky130_fd_pr__nfet_01v8 L=0.6 W=1.4 nf=1 ad='int((nf+1)/2) * W/nf * 0.29' as='int((nf+2)/2) * W/nf * 0.29'
+ pd='2*int((nf+1)/2) * (W/nf + 0.29)' ps='2*int((nf+2)/2) * (W/nf + 0.29)' nrd='0.29 / W' nrs='0.29 / W'
+ sa=0 sb=0 sd=0 mult=1 m=1
XM74 net8 bias_e net9 VSS sky130_fd_pr__nfet_01v8 L=0.6 W=1.4 nf=1 ad='int((nf+1)/2) * W/nf * 0.29' as='int((nf+2)/2) * W/nf * 0.29'
+ pd='2*int((nf+1)/2) * (W/nf + 0.29)' ps='2*int((nf+2)/2) * (W/nf + 0.29)' nrd='0.29 / W' nrs='0.29 / W'
+ sa=0 sb=0 sd=0 mult=1 m=1
XM75 net9 bias_e VSS VSS sky130_fd_pr__nfet_01v8 L=0.6 W=1.4 nf=1 ad='int((nf+1)/2) * W/nf * 0.29' as='int((nf+2)/2) * W/nf * 0.29'
+ pd='2*int((nf+1)/2) * (W/nf + 0.29)' ps='2*int((nf+2)/2) * (W/nf + 0.29)' nrd='0.29 / W' nrs='0.29 / W'
+ sa=0 sb=0 sd=0 mult=1 m=1
XM76 bias_e bias_e net10 VSS sky130_fd_pr__nfet_01v8 L=0.6 W=1.4 nf=1 ad='int((nf+1)/2) * W/nf * 0.29'
+ as='int((nf+2)/2) * W/nf * 0.29' pd='2*int((nf+1)/2) * (W/nf + 0.29)' ps='2*int((nf+2)/2) * (W/nf + 0.29)'
+ nrd='0.29 / W' nrs='0.29 / W' sa=0 sb=0 sd=0 mult=1 m=1
XM77 net10 bias_e net11 VSS sky130_fd_pr__nfet_01v8 L=0.6 W=1.4 nf=1 ad='int((nf+1)/2) * W/nf * 0.29'
+ as='int((nf+2)/2) * W/nf * 0.29' pd='2*int((nf+1)/2) * (W/nf + 0.29)' ps='2*int((nf+2)/2) * (W/nf + 0.29)'
+ nrd='0.29 / W' nrs='0.29 / W' sa=0 sb=0 sd=0 mult=1 m=1
XM78 net11 bias_e net12 VSS sky130_fd_pr__nfet_01v8 L=0.6 W=1.4 nf=1 ad='int((nf+1)/2) * W/nf * 0.29'
+ as='int((nf+2)/2) * W/nf * 0.29' pd='2*int((nf+1)/2) * (W/nf + 0.29)' ps='2*int((nf+2)/2) * (W/nf + 0.29)'
+ nrd='0.29 / W' nrs='0.29 / W' sa=0 sb=0 sd=0 mult=1 m=1
XM79 net12 bias_e VSS VSS sky130_fd_pr__nfet_01v8 L=0.6 W=1.4 nf=1 ad='int((nf+1)/2) * W/nf * 0.29' as='int((nf+2)/2) * W/nf * 0.29'
+ pd='2*int((nf+1)/2) * (W/nf + 0.29)' ps='2*int((nf+2)/2) * (W/nf + 0.29)' nrd='0.29 / W' nrs='0.29 / W'
+ sa=0 sb=0 sd=0 mult=1 m=1
XM64 bias_e bias_e net13 VSS sky130_fd_pr__nfet_01v8 L=0.6 W=1.4 nf=1 ad='int((nf+1)/2) * W/nf * 0.29'
+ as='int((nf+2)/2) * W/nf * 0.29' pd='2*int((nf+1)/2) * (W/nf + 0.29)' ps='2*int((nf+2)/2) * (W/nf + 0.29)'
+ nrd='0.29 / W' nrs='0.29 / W' sa=0 sb=0 sd=0 mult=1 m=1
XM65 net13 bias_e net14 VSS sky130_fd_pr__nfet_01v8 L=0.6 W=1.4 nf=1 ad='int((nf+1)/2) * W/nf * 0.29'
+ as='int((nf+2)/2) * W/nf * 0.29' pd='2*int((nf+1)/2) * (W/nf + 0.29)' ps='2*int((nf+2)/2) * (W/nf + 0.29)'
+ nrd='0.29 / W' nrs='0.29 / W' sa=0 sb=0 sd=0 mult=1 m=1
XM66 net14 bias_e net15 VSS sky130_fd_pr__nfet_01v8 L=0.6 W=1.4 nf=1 ad='int((nf+1)/2) * W/nf * 0.29'
+ as='int((nf+2)/2) * W/nf * 0.29' pd='2*int((nf+1)/2) * (W/nf + 0.29)' ps='2*int((nf+2)/2) * (W/nf + 0.29)'
+ nrd='0.29 / W' nrs='0.29 / W' sa=0 sb=0 sd=0 mult=1 m=1
XM67 net15 bias_e VSS VSS sky130_fd_pr__nfet_01v8 L=0.6 W=1.4 nf=1 ad='int((nf+1)/2) * W/nf * 0.29' as='int((nf+2)/2) * W/nf * 0.29'
+ pd='2*int((nf+1)/2) * (W/nf + 0.29)' ps='2*int((nf+2)/2) * (W/nf + 0.29)' nrd='0.29 / W' nrs='0.29 / W'
+ sa=0 sb=0 sd=0 mult=1 m=1
XM80 op VSS VSS VSS sky130_fd_pr__nfet_01v8 L=0.6 W=1.4 nf=1 ad='int((nf+1)/2) * W/nf * 0.29' as='int((nf+2)/2) * W/nf * 0.29'
+ pd='2*int((nf+1)/2) * (W/nf + 0.29)' ps='2*int((nf+2)/2) * (W/nf + 0.29)' nrd='0.29 / W' nrs='0.29 / W'
+ sa=0 sb=0 sd=0 mult=2 m=2
XM81 on VSS VSS VSS sky130_fd_pr__nfet_01v8 L=0.6 W=1.4 nf=1 ad='int((nf+1)/2) * W/nf * 0.29' as='int((nf+2)/2) * W/nf * 0.29'
+ pd='2*int((nf+1)/2) * (W/nf + 0.29)' ps='2*int((nf+2)/2) * (W/nf + 0.29)' nrd='0.29 / W' nrs='0.29 / W'
+ sa=0 sb=0 sd=0 mult=2 m=2
**.ends
.GLOBAL VDD
.end
